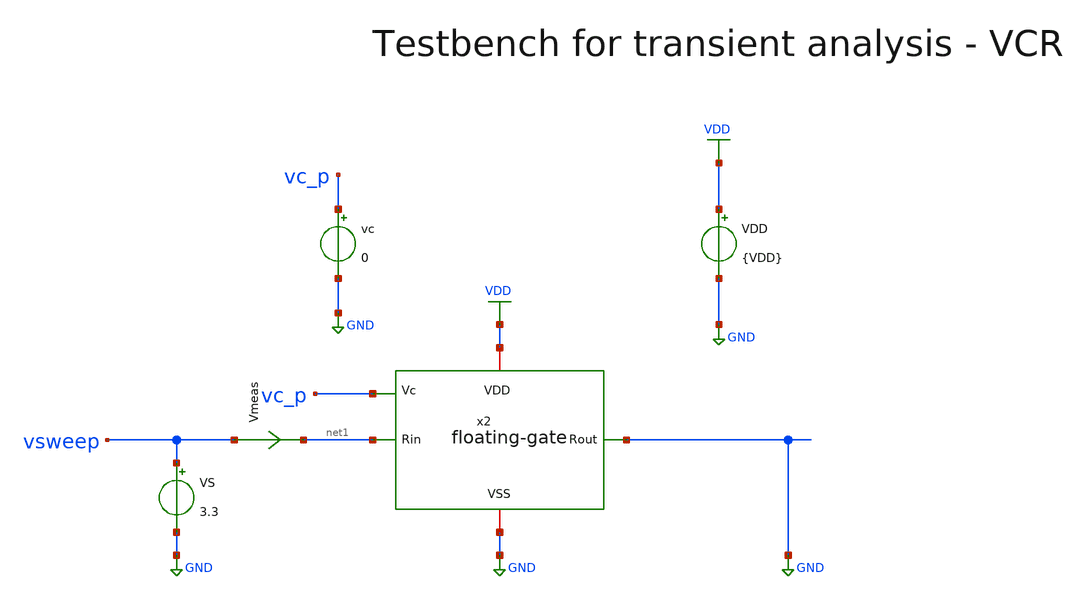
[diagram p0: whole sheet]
** sch_path: macros/heichips26_analog_project/macros/floating-gate/testbenches/xschem/res_tb_linearity.sch
**.subckt res_tb_linearity
VDD VDD GND {VDD}
VS vsweep GND 3.3
Vmeas vsweep net1 0
.save i(vmeas)
vc vc_p GND 0
x2 net1 VDD GND GND vc_p floating-gate
**** begin user architecture code

.lib cornerMOSlv.lib mos_tt
.lib cornerMOShv.lib mos_tt
.lib cornerRES.lib res_typ
.lib cornerDIO.lib dio_tt



* .include ../../../netlist/pex/inverter_magic_pex_3.spice
.param VDD=1.5
.csparam VDD=VDD
.param Vcm=VDD/2
.csparam Vcm=Vcm
.param temp=27
.options savecurrents klu method=gear reltol=1e-3 abstol=1e-15 gmin=1e-15
.control
let vcc = 0.0

save all
set appendwrite



repeat 5
  alter vc $&vcc

  * DC Sweep
  * dc VS -1.5 1.5 1m
  dc VS 0.001 3.3 1m
  remzerovec
  let vcc = vcc + 0.6
end
write @schname\.raw
set appendwrite

* Plotting
plot dc1.v(vsweep)/(dc1.i(Vmeas)) dc2.v(vsweep)/(dc2.i(Vmeas)) dc3.v(vsweep)/(dc3.i(Vmeas))
+ dc4.v(vsweep)/(dc4.i(Vmeas)) dc5.v(vsweep)/(dc5.i(Vmeas))

plot dc1.i(Vmeas) dc2.i(Vmeas) dc3.i(Vmeas) dc4.i(Vmeas) dc5.i(Vmeas)

* Write Data
unset appendwrite
set wr_vecnames
set wr_singlescale

wrdata ../plot_simulations/data/@schname\.txt dc1.v(vsweep)/dc1.i(Vmeas) dc2.v(vsweep)/dc2.i(Vmeas)
+ dc3.v(vsweep)/dc3.i(Vmeas) dc4.v(vsweep)/dc4.i(Vmeas) dc5.v(vsweep)/dc5.i(Vmeas)


*quit
.endc


**** end user architecture code
**.ends

* expanding   symbol:  floating-gate.sym # of pins=5
** sym_path: macros/heichips26_analog_project/macros/floating-gate/schematic/xschem/floating-gate.sym
** sch_path: macros/heichips26_analog_project/macros/floating-gate/schematic/xschem/floating-gate.sch
.subckt floating-gate Rin VDD VSS Rout Vc
*.iopin VDD
*.ipin Rin
*.opin Rout
*.ipin Vc
*.iopin VSS
XM1 Rin Vc Rout VSS sg13_lv_nmos w=2u l=0.13u ng=1 m=1 mm_ok=1
XM2 Rin Rin net1 VSS sg13_lv_nmos w=0.5u l=0.13u ng=1 m=1 mm_ok=1
XM3 VDD VDD net1 VSS sg13_lv_nmos w=0.5u l=0.13u ng=1 m=1 mm_ok=1
XM4 net1 Vc Rout VSS sg13_lv_nmos w=2u l=0.13u ng=1 m=1 mm_ok=1
.ends

.GLOBAL GND
.GLOBAL VDD
.end
